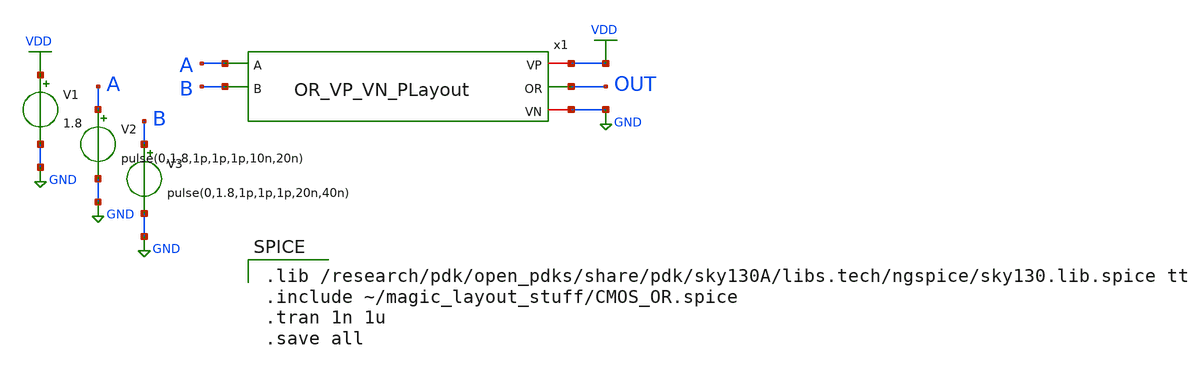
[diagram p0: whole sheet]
** sch_path: skywater_stuff/OR_VP_VN_sim.sch
**.subckt OR_VP_VN_sim
V1 VDD GND 1.8
V2 A GND pulse(0,1.8,1p,1p,1p,10n,20n)
V3 B GND pulse(0,1.8,1p,1p,1p,20n,40n)
x1 VDD A B OUT GND OR_VP_VN_PLayout
**** begin user architecture code

.lib /research/pdk/open_pdks/share/pdk/sky130A/libs.tech/ngspice/sky130.lib.spice tt
.include ~/magic_layout_stuff/CMOS_OR.spice
.tran 1n 1u
.save all

**** end user architecture code
**.ends
.GLOBAL GND
.GLOBAL VDD
.end
